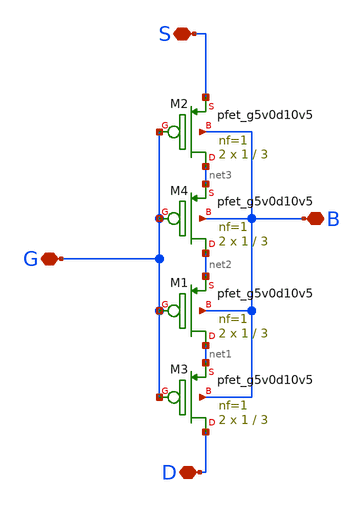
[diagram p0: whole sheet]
** sch_path: xschem/2_p_4_s_1_3.sch
**.subckt 2_p_4_s_1_3 D B G S
*.iopin D
*.iopin B
*.iopin G
*.iopin S
XM1 net1 G net2 B sky130_fd_pr__pfet_g5v0d10v5 L=3 W=1 nf=1 ad='int((nf+1)/2) * W/nf * 0.29' as='int((nf+2)/2) * W/nf * 0.29'
+ pd='2*int((nf+1)/2) * (W/nf + 0.29)' ps='2*int((nf+2)/2) * (W/nf + 0.29)' nrd='0.29 / W' nrs='0.29 / W'
+ sa=0 sb=0 sd=0 mult=2 m=2
XM2 net3 G S B sky130_fd_pr__pfet_g5v0d10v5 L=3 W=1 nf=1 ad='int((nf+1)/2) * W/nf * 0.29' as='int((nf+2)/2) * W/nf * 0.29'
+ pd='2*int((nf+1)/2) * (W/nf + 0.29)' ps='2*int((nf+2)/2) * (W/nf + 0.29)' nrd='0.29 / W' nrs='0.29 / W'
+ sa=0 sb=0 sd=0 mult=2 m=2
XM3 D G net1 B sky130_fd_pr__pfet_g5v0d10v5 L=3 W=1 nf=1 ad='int((nf+1)/2) * W/nf * 0.29' as='int((nf+2)/2) * W/nf * 0.29'
+ pd='2*int((nf+1)/2) * (W/nf + 0.29)' ps='2*int((nf+2)/2) * (W/nf + 0.29)' nrd='0.29 / W' nrs='0.29 / W'
+ sa=0 sb=0 sd=0 mult=2 m=2
XM4 net2 G net3 B sky130_fd_pr__pfet_g5v0d10v5 L=3 W=1 nf=1 ad='int((nf+1)/2) * W/nf * 0.29' as='int((nf+2)/2) * W/nf * 0.29'
+ pd='2*int((nf+1)/2) * (W/nf + 0.29)' ps='2*int((nf+2)/2) * (W/nf + 0.29)' nrd='0.29 / W' nrs='0.29 / W'
+ sa=0 sb=0 sd=0 mult=2 m=2
**.ends
.end
